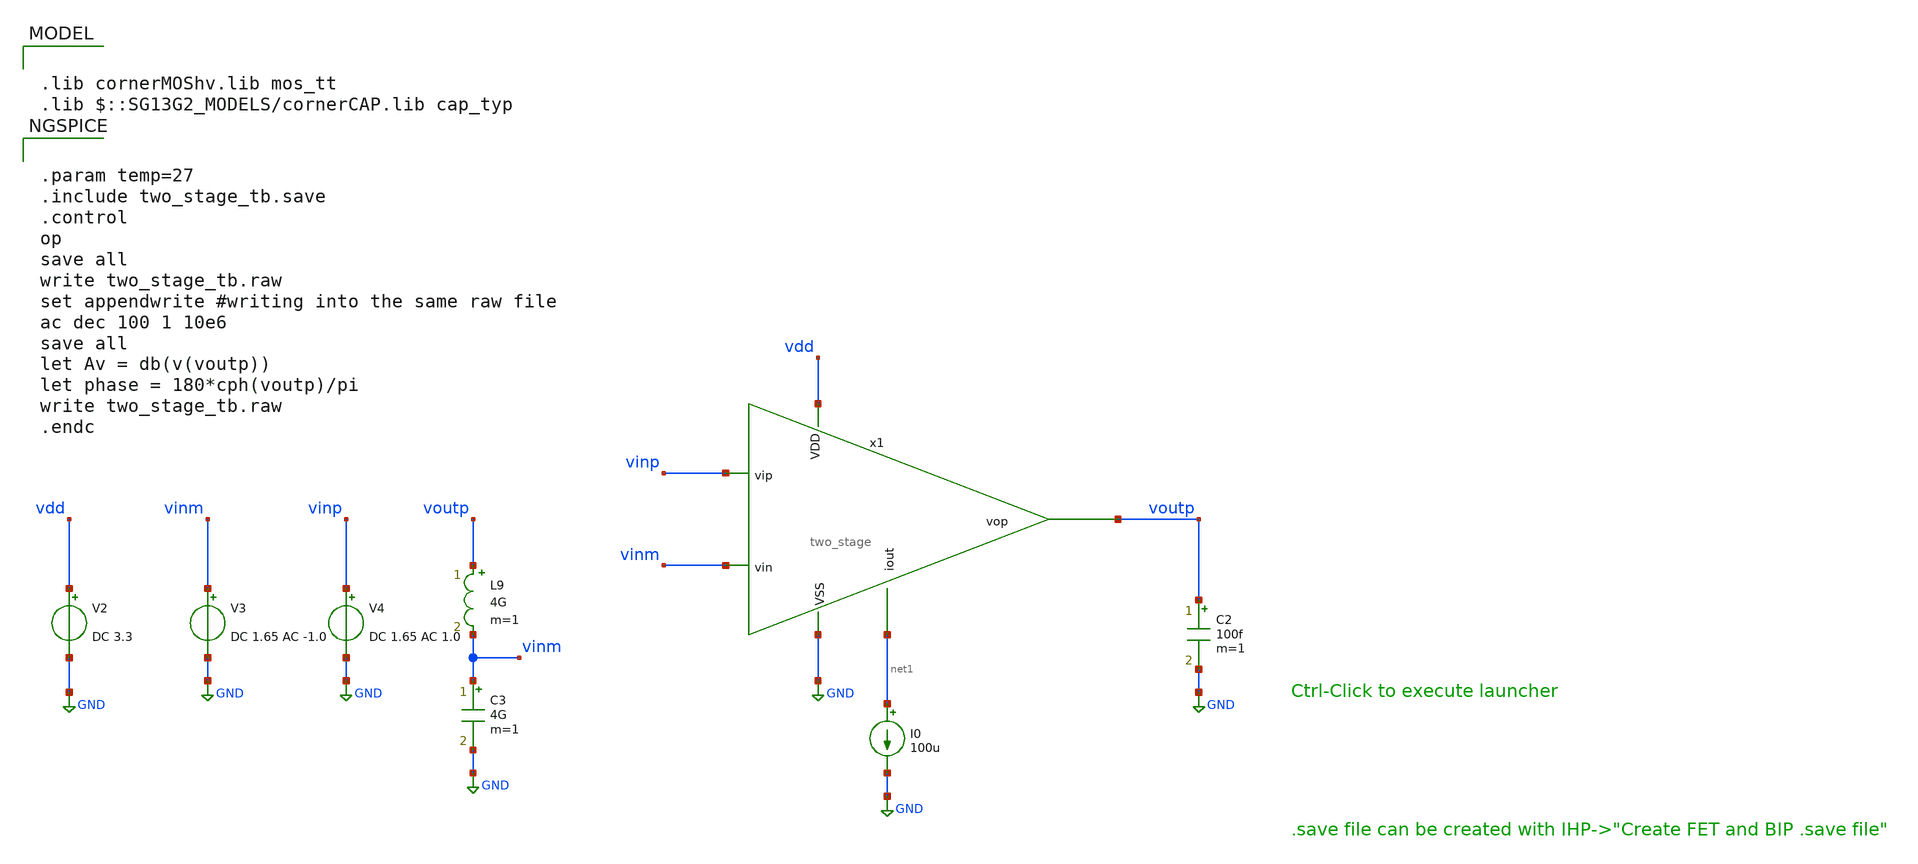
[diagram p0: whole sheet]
** sch_path: testbench/two_stage_tb.sch
**.subckt two_stage_tb
C2 voutp GND 100f m=1
V2 vdd GND DC 3.3
V3 vinm GND DC 1.65 AC -1.0
V4 vinp GND DC 1.65 AC 1.0
L9 voutp vinm 4G m=1
C3 vinm GND 4G m=1
x1 vdd voutp vinp vinm GND net1 two_stage
I0 net1 GND 100u
**** begin user architecture code

.lib cornerMOShv.lib mos_tt
.lib $::SG13G2_MODELS/cornerCAP.lib cap_typ



.param temp=27
.include two_stage_tb.save
.control
op
save all
write two_stage_tb.raw
set appendwrite #writing into the same raw file
ac dec 100 1 10e6
save all
let Av = db(v(voutp))
let phase = 180*cph(voutp)/pi
write two_stage_tb.raw
.endc


**** end user architecture code
**.ends

* expanding   symbol:  two_stage.sym # of pins=6
** sym_path: schematic/two_stage.sym
** sch_path: schematic/two_stage.sch
.subckt two_stage vdd out v+ v- vss iout
*.opin out
*.ipin iout
*.ipin v-
*.ipin v+
*.ipin vdd
*.ipin vss
XM1 net2 v- net1 vdd sg13_hv_pmos w=0.3u l=0.4u ng=1 m=1 mm_ok=1
XM2 net3 v+ net1 vdd sg13_hv_pmos w=0.3u l=0.4u ng=1 m=1 mm_ok=1
XM5 mirror vb_n net5 vss sg13_hv_nmos w=0.3u l=0.45u ng=1 m=1 mm_ok=1
XM11 net1 iout vdd vdd sg13_hv_pmos w=0.3u l=0.4u ng=1 m=1 mm_ok=1
XM12 iout iout vdd vdd sg13_hv_pmos w=0.3u l=0.4u ng=1 m=1 mm_ok=1
XM3 mirror vb_p net2 vdd sg13_hv_pmos w=0.3u l=0.4u ng=1 m=1 mm_ok=1
XM4 net4 vb_p net3 vdd sg13_hv_pmos w=0.3u l=0.4u ng=1 m=1 mm_ok=1
XM6 net4 vb_n net6 vss sg13_hv_nmos w=0.3u l=0.45u ng=1 m=1 mm_ok=1
XM7 net5 mirror vss vss sg13_hv_nmos w=0.3u l=0.45u ng=1 m=1 mm_ok=1
XM8 net6 mirror vss vss sg13_hv_nmos w=0.3u l=0.45u ng=1 m=1 mm_ok=1
XM9 out net4 vss vss sg13_hv_nmos w=0.3u l=0.45u ng=1 m=1 mm_ok=1
XC1 net4 out cap_cmim w=7.0e-6 l=7.0e-6 m=1 mm_ok=1
XM10 out iout vdd vdd sg13_hv_pmos w=0.3u l=0.4u ng=1 m=1 mm_ok=1
V1 vb_p vss 1.5
V2 vb_n vss 1.5
.ends

.GLOBAL GND
.end
